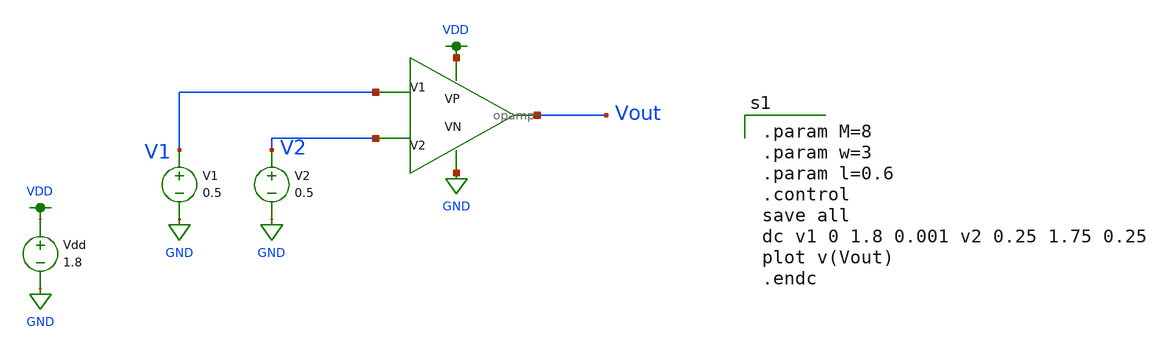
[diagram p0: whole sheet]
** sch_path: schematics/opamp_testbench.sch
**.subckt opamp_testbench
Vdd VDD GND 1.8
V1 V1 GND 0.5
V2 V2 GND 0.5
X1 V1 V2 VDD GND Vout opamp
**** begin user architecture code

.option wnflag=1
.param MC_SWITCH=0.0
.lib ~/skywater/skywater-pdk/libraries/sky130_fd_pr_ngspice/latest/models/sky130.lib.spice tt


.param M=8
.param w=3
.param l=0.6
.control
save all
dc v1 0 1.8 0.001 v2 0.25 1.75 0.25
plot v(Vout)
.endc

**** end user architecture code
**.ends

* expanding   symbol:  /home/madvlsi/Desktop/MADVLSI_final/schematics/opamp.sym # of pins=5
** sym_path: schematics/opamp.sym
** sch_path: schematics/opamp.sch
.subckt opamp V1 V2 VP VN Vout
*.ipin V1
*.ipin V2
*.opin Vout
*.iopin VP
*.iopin VN
*.iopin VP
*.iopin VN
XM1 VN net6 net2 GND sky130_fd_pr__nfet_01v8 L=l W=w nf=1 ad='int((nf+1)/2) * W/nf * 0.29' as='int((nf+2)/2) * W/nf * 0.29'
+ pd='2*int((nf+1)/2) * (W/nf + 0.29)' ps='2*int((nf+2)/2) * (W/nf + 0.29)' nrd='0.29 / W' nrs='0.29 / W'
+ sa=0 sb=0 sd=0 mult=1 m=1
XM2 VP net3 net1 VDD sky130_fd_pr__pfet_01v8 L=l W=w nf=1 ad='int((nf+1)/2) * W/nf * 0.29' as='int((nf+2)/2) * W/nf * 0.29'
+ pd='2*int((nf+1)/2) * (W/nf + 0.29)' ps='2*int((nf+2)/2) * (W/nf + 0.29)' nrd='0.29 / W' nrs='0.29 / W'
+ sa=0 sb=0 sd=0 mult=1 m=1
XM3 net1 V2 Vd VDD sky130_fd_pr__pfet_01v8 L=l W=w nf=1 ad='int((nf+1)/2) * W/nf * 0.29' as='int((nf+2)/2) * W/nf * 0.29'
+ pd='2*int((nf+1)/2) * (W/nf + 0.29)' ps='2*int((nf+2)/2) * (W/nf + 0.29)' nrd='0.29 / W' nrs='0.29 / W'
+ sa=0 sb=0 sd=0 mult=1 m=1
XM4 Vc V1 net1 VDD sky130_fd_pr__pfet_01v8 L=l W=w nf=1 ad='int((nf+1)/2) * W/nf * 0.29' as='int((nf+2)/2) * W/nf * 0.29'
+ pd='2*int((nf+1)/2) * (W/nf + 0.29)' ps='2*int((nf+2)/2) * (W/nf + 0.29)' nrd='0.29 / W' nrs='0.29 / W'
+ sa=0 sb=0 sd=0 mult=1 m=1
XM5 Va V1 net2 GND sky130_fd_pr__nfet_01v8 L=l W=w nf=1 ad='int((nf+1)/2) * W/nf * 0.29' as='int((nf+2)/2) * W/nf * 0.29'
+ pd='2*int((nf+1)/2) * (W/nf + 0.29)' ps='2*int((nf+2)/2) * (W/nf + 0.29)' nrd='0.29 / W' nrs='0.29 / W'
+ sa=0 sb=0 sd=0 mult=1 m=1
XM6 net2 V2 Vb GND sky130_fd_pr__nfet_01v8 L=l W=w nf=1 ad='int((nf+1)/2) * W/nf * 0.29' as='int((nf+2)/2) * W/nf * 0.29'
+ pd='2*int((nf+1)/2) * (W/nf + 0.29)' ps='2*int((nf+2)/2) * (W/nf + 0.29)' nrd='0.29 / W' nrs='0.29 / W'
+ sa=0 sb=0 sd=0 mult=1 m=1
XM7 net3 net3 Va VDD sky130_fd_pr__pfet_01v8 L=l W=w nf=1 ad='int((nf+1)/2) * W/nf * 0.29' as='int((nf+2)/2) * W/nf * 0.29'
+ pd='2*int((nf+1)/2) * (W/nf + 0.29)' ps='2*int((nf+2)/2) * (W/nf + 0.29)' nrd='0.29 / W' nrs='0.29 / W'
+ sa=0 sb=0 sd=0 mult=1 m=1
XM8 net5 net5 Va VDD sky130_fd_pr__pfet_01v8 L=l W=w nf=1 ad='int((nf+1)/2) * W/nf * 0.29' as='int((nf+2)/2) * W/nf * 0.29'
+ pd='2*int((nf+1)/2) * (W/nf + 0.29)' ps='2*int((nf+2)/2) * (W/nf + 0.29)' nrd='0.29 / W' nrs='0.29 / W'
+ sa=0 sb=0 sd=0 mult=1 m=1
XM9 Vout net5 Vb VDD sky130_fd_pr__pfet_01v8 L=l W=w nf=1 ad='int((nf+1)/2) * W/nf * 0.29' as='int((nf+2)/2) * W/nf * 0.29'
+ pd='2*int((nf+1)/2) * (W/nf + 0.29)' ps='2*int((nf+2)/2) * (W/nf + 0.29)' nrd='0.29 / W' nrs='0.29 / W'
+ sa=0 sb=0 sd=0 mult=1 m=1
XM10 Va net3 VP VDD sky130_fd_pr__pfet_01v8 L=l W=w nf=1 ad='int((nf+1)/2) * W/nf * 0.29' as='int((nf+2)/2) * W/nf * 0.29'
+ pd='2*int((nf+1)/2) * (W/nf + 0.29)' ps='2*int((nf+2)/2) * (W/nf + 0.29)' nrd='0.29 / W' nrs='0.29 / W'
+ sa=0 sb=0 sd=0 mult=1 m=1
XM11 Vb net3 VP VDD sky130_fd_pr__pfet_01v8 L=l W=w nf=1 ad='int((nf+1)/2) * W/nf * 0.29' as='int((nf+2)/2) * W/nf * 0.29'
+ pd='2*int((nf+1)/2) * (W/nf + 0.29)' ps='2*int((nf+2)/2) * (W/nf + 0.29)' nrd='0.29 / W' nrs='0.29 / W'
+ sa=0 sb=0 sd=0 mult=1 m=1
XM12 net5 net5 Vc GND sky130_fd_pr__nfet_01v8 L=l W=w nf=1 ad='int((nf+1)/2) * W/nf * 0.29' as='int((nf+2)/2) * W/nf * 0.29'
+ pd='2*int((nf+1)/2) * (W/nf + 0.29)' ps='2*int((nf+2)/2) * (W/nf + 0.29)' nrd='0.29 / W' nrs='0.29 / W'
+ sa=0 sb=0 sd=0 mult=1 m=1
XM13 Vout net5 Vd GND sky130_fd_pr__nfet_01v8 L=l W=w nf=1 ad='int((nf+1)/2) * W/nf * 0.29' as='int((nf+2)/2) * W/nf * 0.29'
+ pd='2*int((nf+1)/2) * (W/nf + 0.29)' ps='2*int((nf+2)/2) * (W/nf + 0.29)' nrd='0.29 / W' nrs='0.29 / W'
+ sa=0 sb=0 sd=0 mult=1 m=1
XM14 Vc net6 VN GND sky130_fd_pr__nfet_01v8 L=l W=w nf=1 ad='int((nf+1)/2) * W/nf * 0.29' as='int((nf+2)/2) * W/nf * 0.29'
+ pd='2*int((nf+1)/2) * (W/nf + 0.29)' ps='2*int((nf+2)/2) * (W/nf + 0.29)' nrd='0.29 / W' nrs='0.29 / W'
+ sa=0 sb=0 sd=0 mult=1 m=1
XM15 Vd net6 VN GND sky130_fd_pr__nfet_01v8 L=l W=w nf=1 ad='int((nf+1)/2) * W/nf * 0.29' as='int((nf+2)/2) * W/nf * 0.29'
+ pd='2*int((nf+1)/2) * (W/nf + 0.29)' ps='2*int((nf+2)/2) * (W/nf + 0.29)' nrd='0.29 / W' nrs='0.29 / W'
+ sa=0 sb=0 sd=0 mult=1 m=1
XM16 net7 net6 net3 GND sky130_fd_pr__nfet_01v8 L=l W=w nf=1 ad='int((nf+1)/2) * W/nf * 0.29' as='int((nf+2)/2) * W/nf * 0.29'
+ pd='2*int((nf+1)/2) * (W/nf + 0.29)' ps='2*int((nf+2)/2) * (W/nf + 0.29)' nrd='0.29 / W' nrs='0.29 / W'
+ sa=0 sb=0 sd=0 mult=1 m=1
XM17 VN net6 net7 GND sky130_fd_pr__nfet_01v8 L=l W=w nf=1 ad='int((nf+1)/2) * W/nf * 0.29' as='int((nf+2)/2) * W/nf * 0.29'
+ pd='2*int((nf+1)/2) * (W/nf + 0.29)' ps='2*int((nf+2)/2) * (W/nf + 0.29)' nrd='0.29 / W' nrs='0.29 / W'
+ sa=0 sb=0 sd=0 mult=1 m=1
XM18 net7 net6 VP GND sky130_fd_pr__nfet_01v8 L=l W=w nf=1 ad='int((nf+1)/2) * W/nf * 0.29' as='int((nf+2)/2) * W/nf * 0.29'
+ pd='2*int((nf+1)/2) * (W/nf + 0.29)' ps='2*int((nf+2)/2) * (W/nf + 0.29)' nrd='0.29 / W' nrs='0.29 / W'
+ sa=0 sb=0 sd=0 mult=M m=M
XM19 net4 net3 net6 VDD sky130_fd_pr__pfet_01v8 L=l W=w nf=1 ad='int((nf+1)/2) * W/nf * 0.29' as='int((nf+2)/2) * W/nf * 0.29'
+ pd='2*int((nf+1)/2) * (W/nf + 0.29)' ps='2*int((nf+2)/2) * (W/nf + 0.29)' nrd='0.29 / W' nrs='0.29 / W'
+ sa=0 sb=0 sd=0 mult=1 m=1
XM20 VP net3 net4 VDD sky130_fd_pr__pfet_01v8 L=l W=w nf=1 ad='int((nf+1)/2) * W/nf * 0.29' as='int((nf+2)/2) * W/nf * 0.29'
+ pd='2*int((nf+1)/2) * (W/nf + 0.29)' ps='2*int((nf+2)/2) * (W/nf + 0.29)' nrd='0.29 / W' nrs='0.29 / W'
+ sa=0 sb=0 sd=0 mult=1 m=1
XM21 net4 net3 VN VDD sky130_fd_pr__pfet_01v8 L=l W=w nf=1 ad='int((nf+1)/2) * W/nf * 0.29' as='int((nf+2)/2) * W/nf * 0.29'
+ pd='2*int((nf+1)/2) * (W/nf + 0.29)' ps='2*int((nf+2)/2) * (W/nf + 0.29)' nrd='0.29 / W' nrs='0.29 / W'
+ sa=0 sb=0 sd=0 mult=M m=M
XM22 net6 net6 Vc GND sky130_fd_pr__nfet_01v8 L=l W=w nf=1 ad='int((nf+1)/2) * W/nf * 0.29' as='int((nf+2)/2) * W/nf * 0.29'
+ pd='2*int((nf+1)/2) * (W/nf + 0.29)' ps='2*int((nf+2)/2) * (W/nf + 0.29)' nrd='0.29 / W' nrs='0.29 / W'
+ sa=0 sb=0 sd=0 mult=1 m=1
**** begin user architecture code

.param M=8
.param w=3
.param l=0.6


**** end user architecture code
.ends

.GLOBAL GND
.GLOBAL VDD
.end
